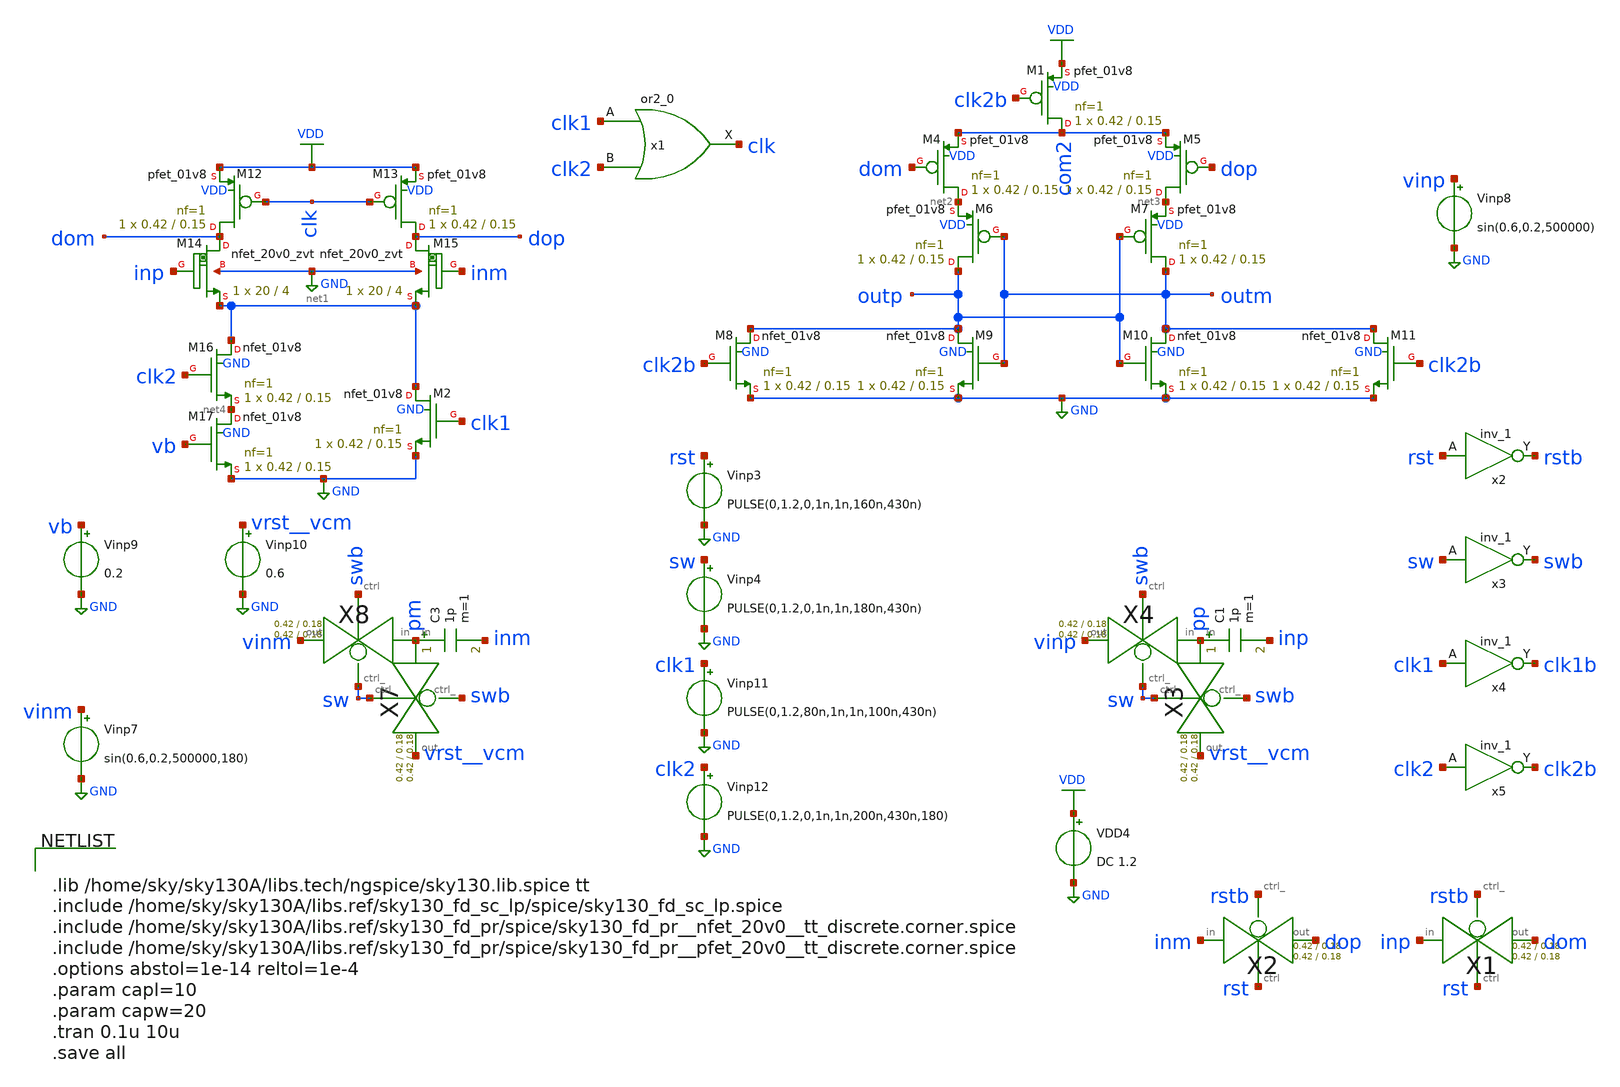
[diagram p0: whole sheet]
** sch_path: xschem/comparator_with_AZ/offsetcancellation.sch
**.subckt offsetcancellation
VDD4 VDD GND DC 1.2
Vinp11 clk1 GND PULSE(0,1.2,80n,1n,1n,100n,430n)
Vinp12 clk2 GND PULSE(0,1.2,0,1n,1n,200n,430n,180)
XM1 com2 clk2b VDD VDD sky130_fd_pr__pfet_01v8 L=0.15 W=0.42 nf=1 ad='int((nf+1)/2) * W/nf * 0.29' as='int((nf+2)/2) * W/nf * 0.29'
+ pd='2*int((nf+1)/2) * (W/nf + 0.29)' ps='2*int((nf+2)/2) * (W/nf + 0.29)' nrd='0.29 / W' nrs='0.29 / W'
+ sa=0 sb=0 sd=0 mult=1 m=1
XM2 net1 clk1 GND GND sky130_fd_pr__nfet_01v8 L=0.15 W=0.42 nf=1 ad='int((nf+1)/2) * W/nf * 0.29' as='int((nf+2)/2) * W/nf * 0.29'
+ pd='2*int((nf+1)/2) * (W/nf + 0.29)' ps='2*int((nf+2)/2) * (W/nf + 0.29)' nrd='0.29 / W' nrs='0.29 / W'
+ sa=0 sb=0 sd=0 mult=1 m=1
XM4 net2 dom com2 VDD sky130_fd_pr__pfet_01v8 L=0.15 W=0.42 nf=1 ad='int((nf+1)/2) * W/nf * 0.29' as='int((nf+2)/2) * W/nf * 0.29'
+ pd='2*int((nf+1)/2) * (W/nf + 0.29)' ps='2*int((nf+2)/2) * (W/nf + 0.29)' nrd='0.29 / W' nrs='0.29 / W'
+ sa=0 sb=0 sd=0 mult=1 m=1
XM5 net3 dop com2 VDD sky130_fd_pr__pfet_01v8 L=0.15 W=0.42 nf=1 ad='int((nf+1)/2) * W/nf * 0.29' as='int((nf+2)/2) * W/nf * 0.29'
+ pd='2*int((nf+1)/2) * (W/nf + 0.29)' ps='2*int((nf+2)/2) * (W/nf + 0.29)' nrd='0.29 / W' nrs='0.29 / W'
+ sa=0 sb=0 sd=0 mult=1 m=1
XM6 outp outm net2 VDD sky130_fd_pr__pfet_01v8 L=0.15 W=0.42 nf=1 ad='int((nf+1)/2) * W/nf * 0.29' as='int((nf+2)/2) * W/nf * 0.29'
+ pd='2*int((nf+1)/2) * (W/nf + 0.29)' ps='2*int((nf+2)/2) * (W/nf + 0.29)' nrd='0.29 / W' nrs='0.29 / W'
+ sa=0 sb=0 sd=0 mult=1 m=1
XM7 outm outp net3 VDD sky130_fd_pr__pfet_01v8 L=0.15 W=0.42 nf=1 ad='int((nf+1)/2) * W/nf * 0.29' as='int((nf+2)/2) * W/nf * 0.29'
+ pd='2*int((nf+1)/2) * (W/nf + 0.29)' ps='2*int((nf+2)/2) * (W/nf + 0.29)' nrd='0.29 / W' nrs='0.29 / W'
+ sa=0 sb=0 sd=0 mult=1 m=1
XM8 outp clk2b GND GND sky130_fd_pr__nfet_01v8 L=0.15 W=0.42 nf=1 ad='int((nf+1)/2) * W/nf * 0.29' as='int((nf+2)/2) * W/nf * 0.29'
+ pd='2*int((nf+1)/2) * (W/nf + 0.29)' ps='2*int((nf+2)/2) * (W/nf + 0.29)' nrd='0.29 / W' nrs='0.29 / W'
+ sa=0 sb=0 sd=0 mult=1 m=1
XM9 outp outm GND GND sky130_fd_pr__nfet_01v8 L=0.15 W=0.42 nf=1 ad='int((nf+1)/2) * W/nf * 0.29' as='int((nf+2)/2) * W/nf * 0.29'
+ pd='2*int((nf+1)/2) * (W/nf + 0.29)' ps='2*int((nf+2)/2) * (W/nf + 0.29)' nrd='0.29 / W' nrs='0.29 / W'
+ sa=0 sb=0 sd=0 mult=1 m=1
XM10 outm outp GND GND sky130_fd_pr__nfet_01v8 L=0.15 W=0.42 nf=1 ad='int((nf+1)/2) * W/nf * 0.29' as='int((nf+2)/2) * W/nf * 0.29'
+ pd='2*int((nf+1)/2) * (W/nf + 0.29)' ps='2*int((nf+2)/2) * (W/nf + 0.29)' nrd='0.29 / W' nrs='0.29 / W'
+ sa=0 sb=0 sd=0 mult=1 m=1
XM11 outm clk2b GND GND sky130_fd_pr__nfet_01v8 L=0.15 W=0.42 nf=1 ad='int((nf+1)/2) * W/nf * 0.29' as='int((nf+2)/2) * W/nf * 0.29'
+ pd='2*int((nf+1)/2) * (W/nf + 0.29)' ps='2*int((nf+2)/2) * (W/nf + 0.29)' nrd='0.29 / W' nrs='0.29 / W'
+ sa=0 sb=0 sd=0 mult=1 m=1
XM12 dom clk VDD VDD sky130_fd_pr__pfet_01v8 L=0.15 W=0.42 nf=1 ad='int((nf+1)/2) * W/nf * 0.29' as='int((nf+2)/2) * W/nf * 0.29'
+ pd='2*int((nf+1)/2) * (W/nf + 0.29)' ps='2*int((nf+2)/2) * (W/nf + 0.29)' nrd='0.29 / W' nrs='0.29 / W'
+ sa=0 sb=0 sd=0 mult=1 m=1
XM13 dop clk VDD VDD sky130_fd_pr__pfet_01v8 L=0.15 W=0.42 nf=1 ad='int((nf+1)/2) * W/nf * 0.29' as='int((nf+2)/2) * W/nf * 0.29'
+ pd='2*int((nf+1)/2) * (W/nf + 0.29)' ps='2*int((nf+2)/2) * (W/nf + 0.29)' nrd='0.29 / W' nrs='0.29 / W'
+ sa=0 sb=0 sd=0 mult=1 m=1
XM14 dom inp net1 GND sky130_fd_pr__nfet_20v0_zvt W=20 L=4 m=1
XM15 dop inm net1 GND sky130_fd_pr__nfet_20v0_zvt W=20 L=4 m=1
XM16 net1 clk2 net4 GND sky130_fd_pr__nfet_01v8 L=0.15 W=0.42 nf=1 ad='int((nf+1)/2) * W/nf * 0.29' as='int((nf+2)/2) * W/nf * 0.29'
+ pd='2*int((nf+1)/2) * (W/nf + 0.29)' ps='2*int((nf+2)/2) * (W/nf + 0.29)' nrd='0.29 / W' nrs='0.29 / W'
+ sa=0 sb=0 sd=0 mult=1 m=1
XM17 net4 vb GND GND sky130_fd_pr__nfet_01v8 L=0.15 W=0.42 nf=1 ad='int((nf+1)/2) * W/nf * 0.29' as='int((nf+2)/2) * W/nf * 0.29'
+ pd='2*int((nf+1)/2) * (W/nf + 0.29)' ps='2*int((nf+2)/2) * (W/nf + 0.29)' nrd='0.29 / W' nrs='0.29 / W'
+ sa=0 sb=0 sd=0 mult=1 m=1
C1 pp inp 1p m=1
X1 inp dom rstb rst transmission_gate Wpmos=0.42 Lpmos=0.18 Wnmos=0.42 Lnmos=0.18
X2 inm dop rstb rst transmission_gate Wpmos=0.42 Lpmos=0.18 Wnmos=0.42 Lnmos=0.18
X3 pp vrst__vcm swb sw transmission_gate Wpmos=0.42 Lpmos=0.18 Wnmos=0.42 Lnmos=0.18
X4 pp vinp sw swb transmission_gate Wpmos=0.42 Lpmos=0.18 Wnmos=0.42 Lnmos=0.18
C3 pm inm 1p m=1
X7 pm vrst__vcm swb sw transmission_gate Wpmos=0.42 Lpmos=0.18 Wnmos=0.42 Lnmos=0.18
X8 pm vinm sw swb transmission_gate Wpmos=0.42 Lpmos=0.18 Wnmos=0.42 Lnmos=0.18
Vinp3 rst GND PULSE(0,1.2,0,1n,1n,160n,430n)
Vinp4 sw GND PULSE(0,1.2,0,1n,1n,180n,430n)
Vinp7 vinm GND sin(0.6,0.2,500000,180)
Vinp8 vinp GND sin(0.6,0.2,500000)
x1 clk1 clk2 GND GND VDD VDD clk sky130_fd_sc_lp__or2_0
Vinp9 vb GND 0.2
Vinp10 vrst__vcm GND 0.6
x2 rst GND GND VDD VDD rstb sky130_fd_sc_lp__inv_1
x3 sw GND GND VDD VDD swb sky130_fd_sc_lp__inv_1
x4 clk1 GND GND VDD VDD clk1b sky130_fd_sc_lp__inv_1
x5 clk2 GND GND VDD VDD clk2b sky130_fd_sc_lp__inv_1
**** begin user architecture code


.lib /home/sky/sky130A/libs.tech/ngspice/sky130.lib.spice tt
.include /home/sky/sky130A/libs.ref/sky130_fd_sc_lp/spice/sky130_fd_sc_lp.spice
.include /home/sky/sky130A/libs.ref/sky130_fd_pr/spice/sky130_fd_pr__nfet_20v0__tt_discrete.corner.spice
.include /home/sky/sky130A/libs.ref/sky130_fd_pr/spice/sky130_fd_pr__pfet_20v0__tt_discrete.corner.spice
.options abstol=1e-14 reltol=1e-4
.param capl=10
.param capw=20
.tran 0.1u 10u
.save all


**** end user architecture code
**.ends

* expanding   symbol:  transmission_gate/transmission_gate.sym # of pins=4
** sym_path: xschem/transmission_gate/transmission_gate.sym
** sch_path: xschem/transmission_gate/transmission_gate.sch
.subckt transmission_gate in out ctrl_ ctrl  Wpmos=0.42 Lpmos=0.18 Wnmos=0.42 Lnmos=0.18
*.iopin in
*.iopin out
*.ipin ctrl_
*.ipin ctrl
XM1 out ctrl in GND sky130_fd_pr__nfet_01v8 L=Lnmos W=Wnmos nf=1 ad='int((nf+1)/2) * W/nf * 0.29' as='int((nf+2)/2) * W/nf * 0.29'
+ pd='2*int((nf+1)/2) * (W/nf + 0.29)' ps='2*int((nf+2)/2) * (W/nf + 0.29)' nrd='0.29 / W' nrs='0.29 / W'
+ sa=0 sb=0 sd=0 mult=1 m=1
XM2 out ctrl_ in VDD sky130_fd_pr__pfet_01v8 L=Lpmos W=Wpmos nf=1 ad='int((nf+1)/2) * W/nf * 0.29' as='int((nf+2)/2) * W/nf * 0.29'
+ pd='2*int((nf+1)/2) * (W/nf + 0.29)' ps='2*int((nf+2)/2) * (W/nf + 0.29)' nrd='0.29 / W' nrs='0.29 / W'
+ sa=0 sb=0 sd=0 mult=1 m=1
.ends

.GLOBAL GND
.GLOBAL VDD
.end
